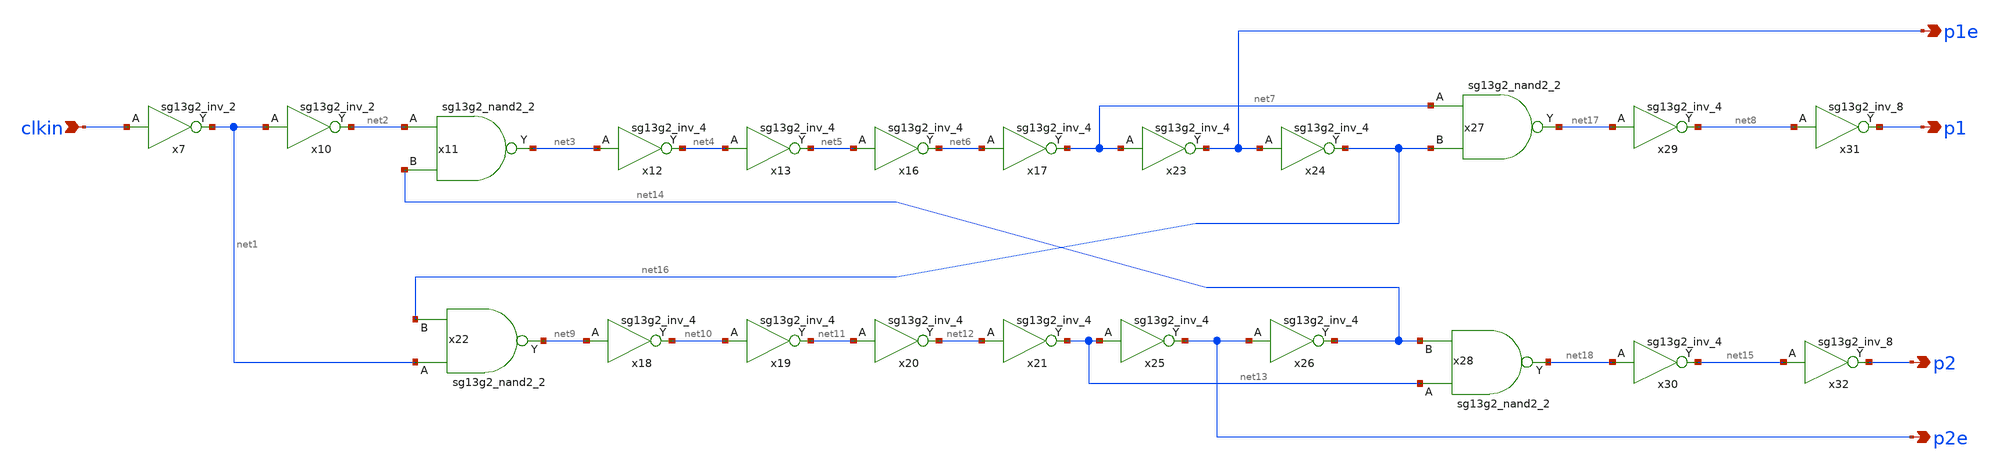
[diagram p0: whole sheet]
** sch_path: 5_Design/4_Layout/Team 3/xschem/clkgen_Team3.sch
* IHP-GmbH/IHP-Open-PDK/ihp-sg13g2/libs.tech/xschem/sg13g2_stdcells/sg13g2_inv_2.sch:
* Copyright 2023 IHP PDK Authors
* Licensed under the Apache License, Version 2.0 (the "License");
**.subckt clkgen_Team3 clkin p1e p2e p1 p2
*.ipin clkin
*.opin p1e
*.opin p2e
*.opin p1
*.opin p2
x7 net1 clkin VDD VSS sg13g2_inv_2
x10 net2 net1 VDD VSS sg13g2_inv_2
x11 net3 net2 net14 VDD VSS sg13g2_nand2_2
x12 net4 net3 VDD VSS sg13g2_inv_4
x13 net5 net4 VDD VSS sg13g2_inv_4
x16 net6 net5 VDD VSS sg13g2_inv_4
x17 net7 net6 VDD VSS sg13g2_inv_4
x18 net10 net9 VDD VSS sg13g2_inv_4
x19 net11 net10 VDD VSS sg13g2_inv_4
x20 net12 net11 VDD VSS sg13g2_inv_4
x21 net13 net12 VDD VSS sg13g2_inv_4
x22 net9 net1 net16 VDD VSS sg13g2_nand2_2
x23 p1e net7 VDD VSS sg13g2_inv_4
x24 net16 p1e VDD VSS sg13g2_inv_4
x25 p2e net13 VDD VSS sg13g2_inv_4
x26 net14 p2e VDD VSS sg13g2_inv_4
x27 net17 net7 net16 VDD VSS sg13g2_nand2_2
x28 net18 net13 net14 VDD VSS sg13g2_nand2_2
x29 net8 net17 VDD VSS sg13g2_inv_4
x30 net15 net18 VDD VSS sg13g2_inv_4
x31 p1 net8 VDD VSS sg13g2_inv_8
x32 p2 net15 VDD VSS sg13g2_inv_8
**.ends

* expanding   symbol:  sg13g2_stdcells/sg13g2_inv_2.sym # of pins=2
** sym_path: sg13g2_stdcells/sg13g2_inv_2.sym
** sch_path: sg13g2_stdcells/sg13g2_inv_2.sch
.subckt sg13g2_inv_2 Y A VDD VSS
*.opin Y
*.ipin A
*.iopin VDD
*.iopin VSS
XM1 Y A VSS VSS sg13_lv_nmos w=1.48u l=130.00n ng=2 m=1 mm_ok=1
XM2 Y A VDD VDD sg13_lv_pmos w=2.24u l=130.00n ng=2 m=1 mm_ok=1
.ends


* expanding   symbol:  sg13g2_stdcells/sg13g2_nand2_2.sym # of pins=3
** sym_path: sg13g2_stdcells/sg13g2_nand2_2.sym
** sch_path: sg13g2_stdcells/sg13g2_nand2_2.sch
.subckt sg13g2_nand2_2 Y A B VDD VSS
*.iopin VDD
*.iopin VSS
*.opin Y
*.ipin B
*.ipin A
XM1 Y A net1 VSS sg13_lv_nmos w=1.44u l=130.00n ng=2 m=1 mm_ok=1
XM2 net1 B VSS VSS sg13_lv_nmos w=1.44u l=130.00n ng=2 m=1 mm_ok=1
XM3 Y A VDD VDD sg13_lv_pmos w=2.24u l=130.00n ng=2 m=1 mm_ok=1
XM4 Y B VDD VDD sg13_lv_pmos w=2.24u l=130.00n ng=2 m=1 mm_ok=1
.ends


* expanding   symbol:  sg13g2_stdcells/sg13g2_inv_4.sym # of pins=2
** sym_path: sg13g2_stdcells/sg13g2_inv_4.sym
** sch_path: sg13g2_stdcells/sg13g2_inv_4.sch
.subckt sg13g2_inv_4 Y A VDD VSS
*.ipin A
*.opin Y
*.iopin VDD
*.iopin VSS
XM1 Y A VSS VSS sg13_lv_nmos w=2.96u l=130.00n ng=4 m=1 mm_ok=1
XM2 Y A VDD VDD sg13_lv_pmos w=4.48u l=130.00n ng=4 m=1 mm_ok=1
.ends


* expanding   symbol:  sg13g2_stdcells/sg13g2_inv_8.sym # of pins=2
** sym_path: sg13g2_stdcells/sg13g2_inv_8.sym
** sch_path: sg13g2_stdcells/sg13g2_inv_8.sch
.subckt sg13g2_inv_8 Y A VDD VSS
*.opin Y
*.ipin A
*.iopin VDD
*.iopin VSS
XM1 Y A VSS VSS sg13_lv_nmos w=5.92u l=130.00n ng=8 m=1 mm_ok=1
XM2 Y A VDD VDD sg13_lv_pmos w=8.96u l=130.00n ng=8 m=1 mm_ok=1
.ends

.end
